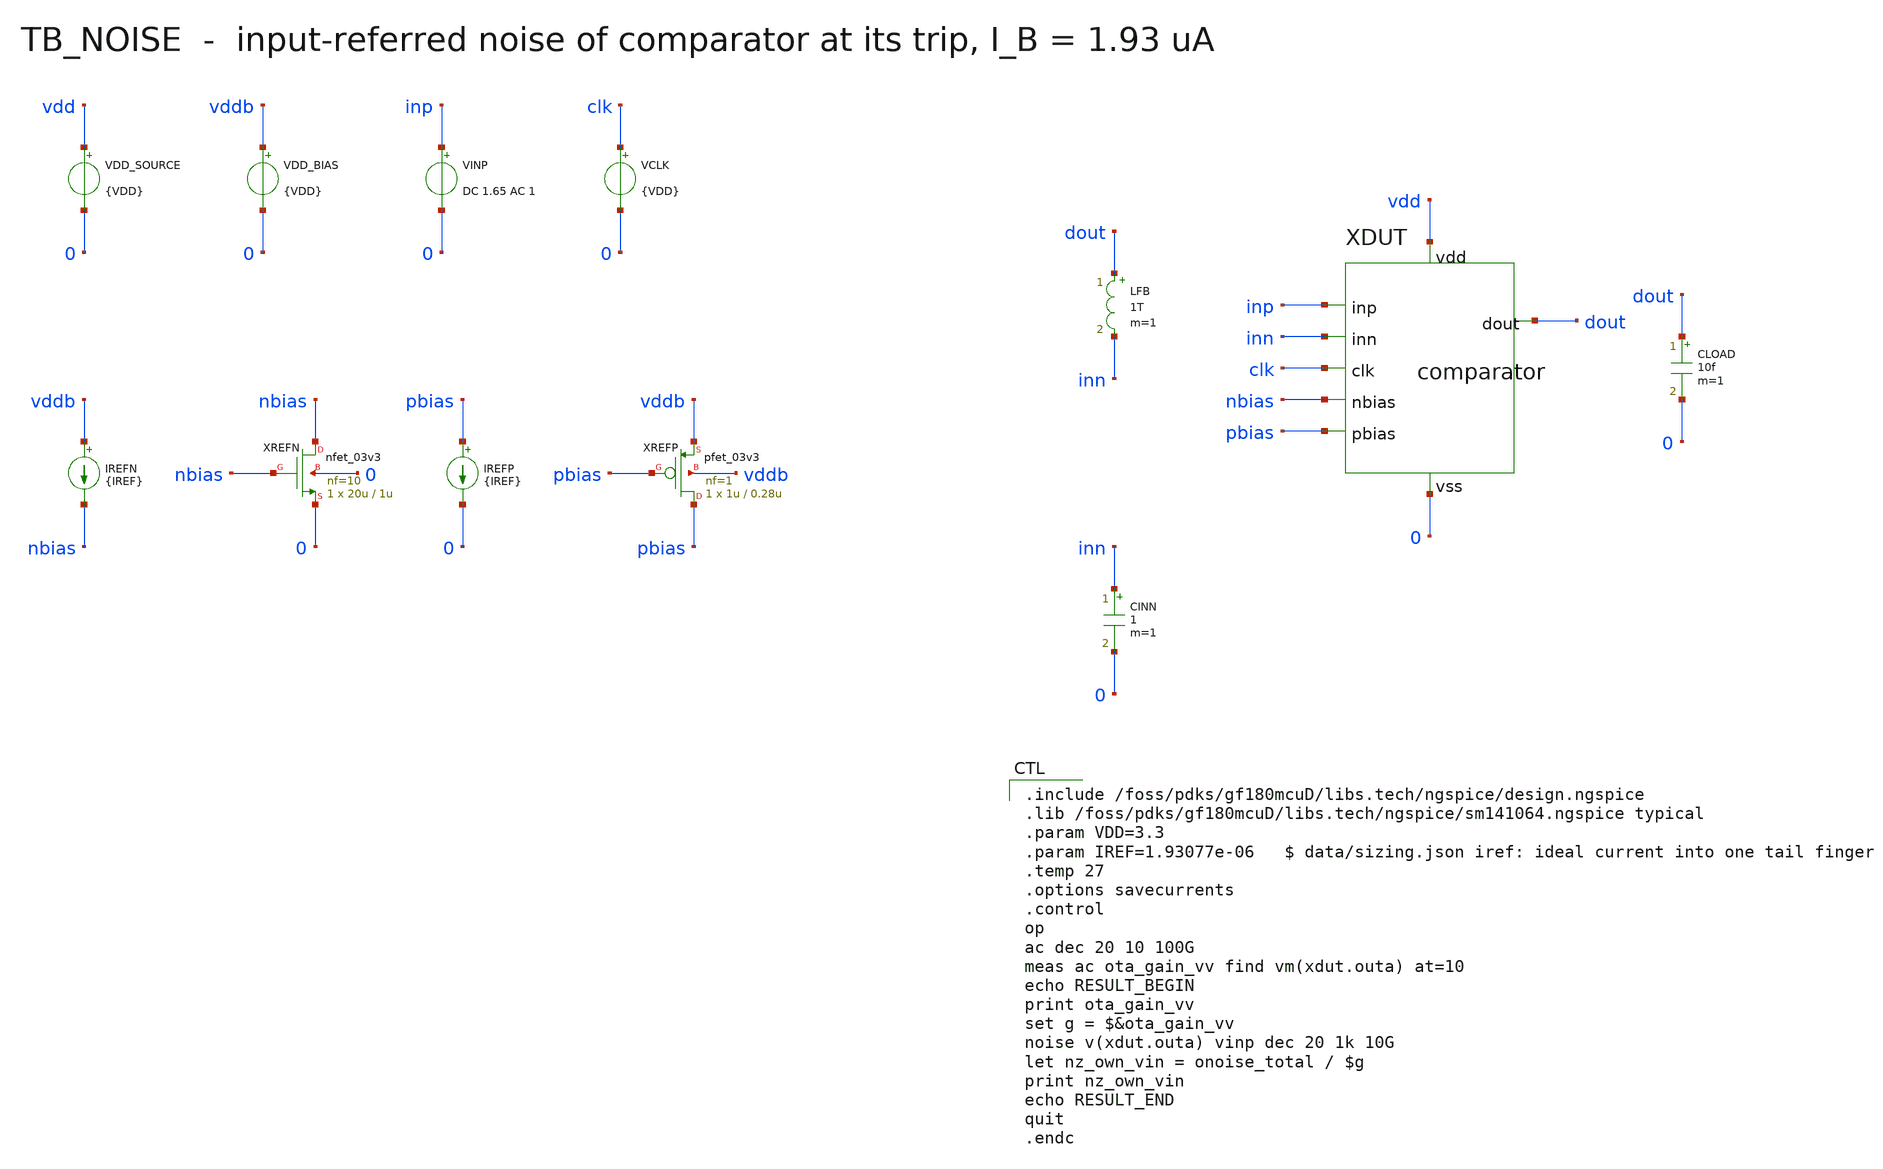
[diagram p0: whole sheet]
** sch_path: mixed_signal/comparator/tb_noise.sch
**.subckt tb_noise
VDD_SOURCE vdd 0 {VDD}
VDD_BIAS vddb 0 {VDD}
VINP inp 0 DC 1.65 AC 1
VCLK clk 0 {VDD}
IREFN vddb nbias {IREF}
XREFN nbias nbias 0 0 nfet_03v3 L=1u W=20u nf=10 ad='int((nf+1)/2) * W/nf * 0.18u' as='int((nf+2)/2) * W/nf * 0.18u'
+ pd='2*int((nf+1)/2) * (W/nf + 0.18u)' ps='2*int((nf+2)/2) * (W/nf + 0.18u)' nrd='0.18u / W' nrs='0.18u / W'
+ sa=0 sb=0 sd=0 m=1
IREFP pbias 0 {IREF}
XREFP pbias pbias vddb vddb pfet_03v3 L=0.28u W=1u nf=1 ad='int((nf+1)/2) * W/nf * 0.18u' as='int((nf+2)/2) * W/nf * 0.18u'
+ pd='2*int((nf+1)/2) * (W/nf + 0.18u)' ps='2*int((nf+2)/2) * (W/nf + 0.18u)' nrd='0.18u / W' nrs='0.18u / W'
+ sa=0 sb=0 sd=0 m=1
CINN inn 0 1 m=1
LFB dout inn 1T m=1
XDUT inp inn dout clk vdd 0 nbias pbias comparator
CLOAD dout 0 10f m=1
**** begin user architecture code

.include /foss/pdks/gf180mcuD/libs.tech/ngspice/design.ngspice
.lib /foss/pdks/gf180mcuD/libs.tech/ngspice/sm141064.ngspice typical
.param VDD=3.3
.param IREF=1.93077e-06   $ data/sizing.json iref: ideal current into one tail finger
.temp 27
.options savecurrents
.control
op
ac dec 20 10 100G
meas ac ota_gain_vv find vm(xdut.outa) at=10
echo RESULT_BEGIN
print ota_gain_vv
set g = $&ota_gain_vv
noise v(xdut.outa) vinp dec 20 1k 10G
let nz_own_vin = onoise_total / $g
print nz_own_vin
echo RESULT_END
quit
.endc

**** end user architecture code
**.ends

* expanding   symbol:  comparator.sym # of pins=8
** sym_path: mixed_signal/comparator/comparator.sym
** sch_path: mixed_signal/comparator/comparator.sch
.subckt comparator inp inn dout clk vdd vss nbias pbias
*.iopin vdd
*.iopin vss
*.ipin pbias
*.ipin inp
*.ipin inn
*.opin dout
*.ipin clk
*.ipin nbias
XTAIL tail pbias vdd vdd pfet_03v3 L=0.28u W=11u nf=11 ad='int((nf+1)/2) * W/nf * 0.18u' as='int((nf+2)/2) * W/nf * 0.18u'
+ pd='2*int((nf+1)/2) * (W/nf + 0.18u)' ps='2*int((nf+2)/2) * (W/nf + 0.18u)' nrd='0.18u / W' nrs='0.18u / W'
+ sa=0 sb=0 sd=0 m=1
XINP left inp tail vdd pfet_03v3 L=0.32u W=12u nf=12 ad='int((nf+1)/2) * W/nf * 0.18u' as='int((nf+2)/2) * W/nf * 0.18u'
+ pd='2*int((nf+1)/2) * (W/nf + 0.18u)' ps='2*int((nf+2)/2) * (W/nf + 0.18u)' nrd='0.18u / W' nrs='0.18u / W'
+ sa=0 sb=0 sd=0 m=1
XINN outa inn tail vdd pfet_03v3 L=0.32u W=12u nf=12 ad='int((nf+1)/2) * W/nf * 0.18u' as='int((nf+2)/2) * W/nf * 0.18u'
+ pd='2*int((nf+1)/2) * (W/nf + 0.18u)' ps='2*int((nf+2)/2) * (W/nf + 0.18u)' nrd='0.18u / W' nrs='0.18u / W'
+ sa=0 sb=0 sd=0 m=1
XLOADD left left vss vss nfet_03v3 L=0.36u W=0.5u nf=1 ad='int((nf+1)/2) * W/nf * 0.18u' as='int((nf+2)/2) * W/nf * 0.18u'
+ pd='2*int((nf+1)/2) * (W/nf + 0.18u)' ps='2*int((nf+2)/2) * (W/nf + 0.18u)' nrd='0.18u / W' nrs='0.18u / W'
+ sa=0 sb=0 sd=0 m=1
XLOADM outa left vss vss nfet_03v3 L=0.36u W=0.5u nf=1 ad='int((nf+1)/2) * W/nf * 0.18u' as='int((nf+2)/2) * W/nf * 0.18u'
+ pd='2*int((nf+1)/2) * (W/nf + 0.18u)' ps='2*int((nf+2)/2) * (W/nf + 0.18u)' nrd='0.18u / W' nrs='0.18u / W'
+ sa=0 sb=0 sd=0 m=1
XBST bst pbias vdd vdd pfet_03v3 L=0.28u W=5u nf=5 ad='int((nf+1)/2) * W/nf * 0.18u' as='int((nf+2)/2) * W/nf * 0.18u'
+ pd='2*int((nf+1)/2) * (W/nf + 0.18u)' ps='2*int((nf+2)/2) * (W/nf + 0.18u)' nrd='0.18u / W' nrs='0.18u / W'
+ sa=0 sb=0 sd=0 m=1
XBUF2 outb outa bst vdd pfet_03v3 L=0.36u W=1u nf=1 ad='int((nf+1)/2) * W/nf * 0.18u' as='int((nf+2)/2) * W/nf * 0.18u'
+ pd='2*int((nf+1)/2) * (W/nf + 0.18u)' ps='2*int((nf+2)/2) * (W/nf + 0.18u)' nrd='0.18u / W' nrs='0.18u / W'
+ sa=0 sb=0 sd=0 m=1
XBUF1 outb outa vss vss nfet_03v3 L=0.36u W=0.5u nf=1 ad='int((nf+1)/2) * W/nf * 0.18u' as='int((nf+2)/2) * W/nf * 0.18u'
+ pd='2*int((nf+1)/2) * (W/nf + 0.18u)' ps='2*int((nf+2)/2) * (W/nf + 0.18u)' nrd='0.18u / W' nrs='0.18u / W'
+ sa=0 sb=0 sd=0 m=1
XBUF4 dout outb vdd vdd pfet_03v3 L=0.36u W=1u nf=1 ad='int((nf+1)/2) * W/nf * 0.18u' as='int((nf+2)/2) * W/nf * 0.18u'
+ pd='2*int((nf+1)/2) * (W/nf + 0.18u)' ps='2*int((nf+2)/2) * (W/nf + 0.18u)' nrd='0.18u / W' nrs='0.18u / W'
+ sa=0 sb=0 sd=0 m=1
XBUF3 dout outb vss vss nfet_03v3 L=0.36u W=0.5u nf=1 ad='int((nf+1)/2) * W/nf * 0.18u' as='int((nf+2)/2) * W/nf * 0.18u'
+ pd='2*int((nf+1)/2) * (W/nf + 0.18u)' ps='2*int((nf+2)/2) * (W/nf + 0.18u)' nrd='0.18u / W' nrs='0.18u / W'
+ sa=0 sb=0 sd=0 m=1
.ends

.end
